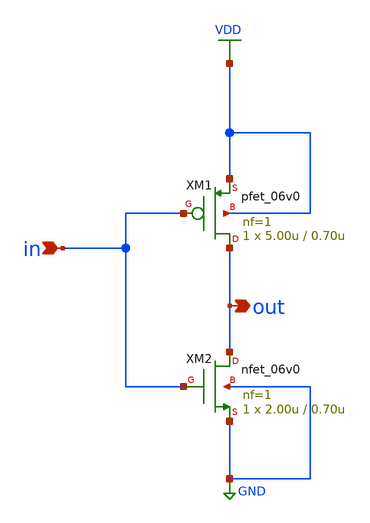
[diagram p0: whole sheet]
** sch_path: member_project/ajisai/inv.sch
**.subckt inv in out
*.ipin in
*.opin out
XM1 out in VDD VDD pfet_06v0 L=0.70u W=5.00u nf=1 ad='int((nf+1)/2) * W/nf * 0.18u' as='int((nf+2)/2) * W/nf * 0.18u'
+ pd='2*int((nf+1)/2) * (W/nf + 0.18u)' ps='2*int((nf+2)/2) * (W/nf + 0.18u)' nrd='0.18u / W' nrs='0.18u / W'
+ sa=0 sb=0 sd=0 m=1
XM2 out in GND GND nfet_06v0 L=0.70u W=2.00u nf=1 ad='int((nf+1)/2) * W/nf * 0.18u' as='int((nf+2)/2) * W/nf * 0.18u'
+ pd='2*int((nf+1)/2) * (W/nf + 0.18u)' ps='2*int((nf+2)/2) * (W/nf + 0.18u)' nrd='0.18u / W' nrs='0.18u / W'
+ sa=0 sb=0 sd=0 m=1
**.ends
.GLOBAL GND
.GLOBAL VDD
.end
